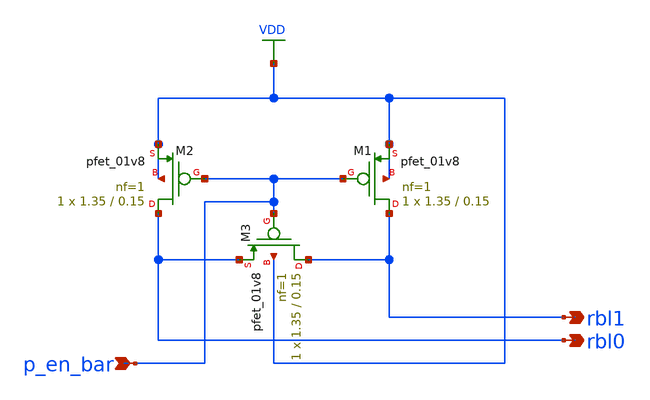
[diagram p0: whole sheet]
** sch_path: xschem/precharge.sch
**.subckt precharge p_en_bar rbl0 rbl1
*.ipin p_en_bar
*.opin rbl0
*.opin rbl1
XM1 rbl1 p_en_bar VDD VDD sky130_fd_pr__pfet_01v8 L=0.15 W=1.35 nf=1 ad='int((nf+1)/2) * W/nf * 0.29'
+ as='int((nf+2)/2) * W/nf * 0.29' pd='2*int((nf+1)/2) * (W/nf + 0.29)' ps='2*int((nf+2)/2) * (W/nf + 0.29)'
+ nrd='0.29 / W' nrs='0.29 / W' sa=0 sb=0 sd=0 mult=1 m=1
XM2 rbl0 p_en_bar VDD VDD sky130_fd_pr__pfet_01v8 L=0.15 W=1.35 nf=1 ad='int((nf+1)/2) * W/nf * 0.29'
+ as='int((nf+2)/2) * W/nf * 0.29' pd='2*int((nf+1)/2) * (W/nf + 0.29)' ps='2*int((nf+2)/2) * (W/nf + 0.29)'
+ nrd='0.29 / W' nrs='0.29 / W' sa=0 sb=0 sd=0 mult=1 m=1
XM3 rbl1 p_en_bar rbl0 VDD sky130_fd_pr__pfet_01v8 L=0.15 W=1.35 nf=1 ad='int((nf+1)/2) * W/nf * 0.29'
+ as='int((nf+2)/2) * W/nf * 0.29' pd='2*int((nf+1)/2) * (W/nf + 0.29)' ps='2*int((nf+2)/2) * (W/nf + 0.29)'
+ nrd='0.29 / W' nrs='0.29 / W' sa=0 sb=0 sd=0 mult=1 m=1
**.ends
.GLOBAL VDD
.end
